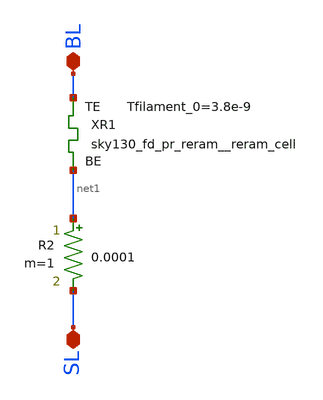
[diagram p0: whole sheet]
** sch_path: xschem/Crossbar/1T1Rres.sch
* StefanSchippers/xschem_sky130/sky130_fd_pr/reram.sym:
* Copyright 2021 Stefan Frederik Schippers
* Licensed under the Apache License, Version 2.0 (the "License");
**.subckt 1T1Rres SL BL
*.iopin SL
*.iopin BL
XR1 BL net1 sky130_fd_pr_reram__reram_cell Tfilament_0=3.8e-9
R2 net1 SL 0.0001 m=1
**.ends
**** begin user architecture code

.subckt sky130_fd_pr_reram__reram_cell TE BE Tfilament_0=3.3e-9 area_ox=0.1024e-12
N1 TE BE nFilament sky130_fd_pr_reram__reram_model
.ic v(nFilament)={Tfilament_0*1.0e9}
.ends sky130_fd_pr_reram__reram_cell

.model sky130_fd_pr_reram__reram_model sky130_fd_pr_reram__reram_module  area_ox = 0.1024e-12  Tox =
+ 5.0  Tfilament_max = 4.9  Tfilament_min = 3.3  Eact_generation = 1.501  Eact_recombination  = 1.500
+  I_k1  = 6.140e-5  Tfilament_ref = 4.7249  V_ref = 0.430  velocity_k1 = 150  gamma_k0  = 16.5  gamma_k1
+  = -1.25  Temperature_0 = 300  C_thermal = 3.1825e-16  tau_thermal = 0.23e-9  t_step  = 1.0e-9
+  smoothing = 1e-7  Kclip = 200

.control
pre_osdi $SKYWATER_MODELS/sky130_fd_pr_reram__reram_module.osdi
.endc

**** end user architecture code
.end
